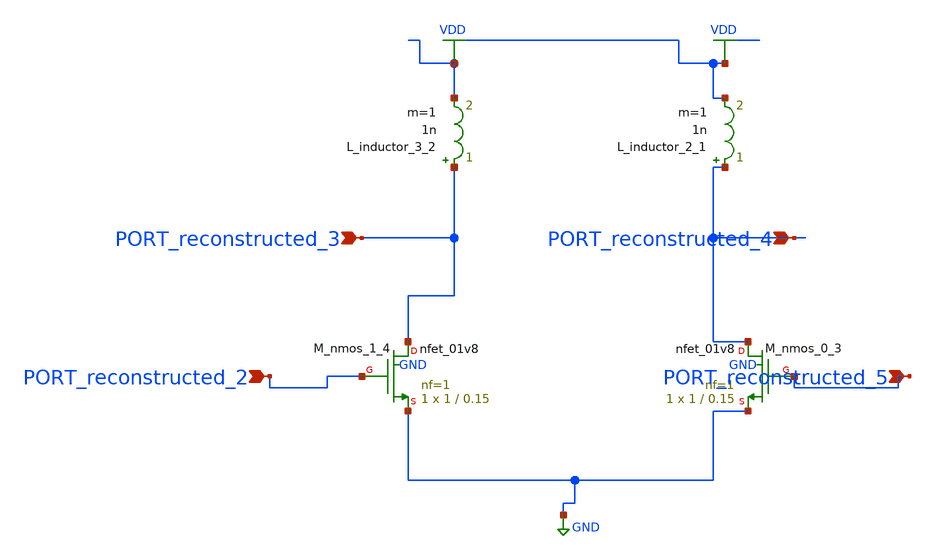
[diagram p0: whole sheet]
** sch_path: schematics/10_1109_ACCESS_2021_3064007_04_002_crop1.sch
**.subckt 10_1109_ACCESS_2021_3064007_04_002_crop1 PORT_reconstructed_3 PORT_reconstructed_4
*+ PORT_reconstructed_5 PORT_reconstructed_2
*.ipin PORT_reconstructed_3
*.ipin PORT_reconstructed_4
*.ipin PORT_reconstructed_5
*.ipin PORT_reconstructed_2
L_inductor_2_1 PORT_reconstructed_4 VDD 1n m=1
L_inductor_3_2 PORT_reconstructed_3 VDD 1n m=1
XM_nmos_0_3 PORT_reconstructed_4 PORT_reconstructed_5 GND GND sky130_fd_pr__nfet_01v8 L=0.15 W=1 nf=1
+ ad='int((1 + 1)/2) * 1 / 1 * 0.29' as='int((1 + 2)/2) * 1 / 1 * 0.29' pd='2*int((1 + 1)/2) * (1 / 1 + 0.29)'
+ ps='2*int((1 + 2)/2) * (1 / 1 + 0.29)' nrd='0.29 / 1 ' nrs='0.29 / 1 ' sa=0 sb=0 sd=0 mult=1 m=1
XM_nmos_1_4 PORT_reconstructed_3 PORT_reconstructed_2 GND GND sky130_fd_pr__nfet_01v8 L=0.15 W=1 nf=1
+ ad='int((1 + 1)/2) * 1 / 1 * 0.29' as='int((1 + 2)/2) * 1 / 1 * 0.29' pd='2*int((1 + 1)/2) * (1 / 1 + 0.29)'
+ ps='2*int((1 + 2)/2) * (1 / 1 + 0.29)' nrd='0.29 / 1 ' nrs='0.29 / 1 ' sa=0 sb=0 sd=0 mult=1 m=1
**.ends
.GLOBAL GND
.GLOBAL VDD
.end
